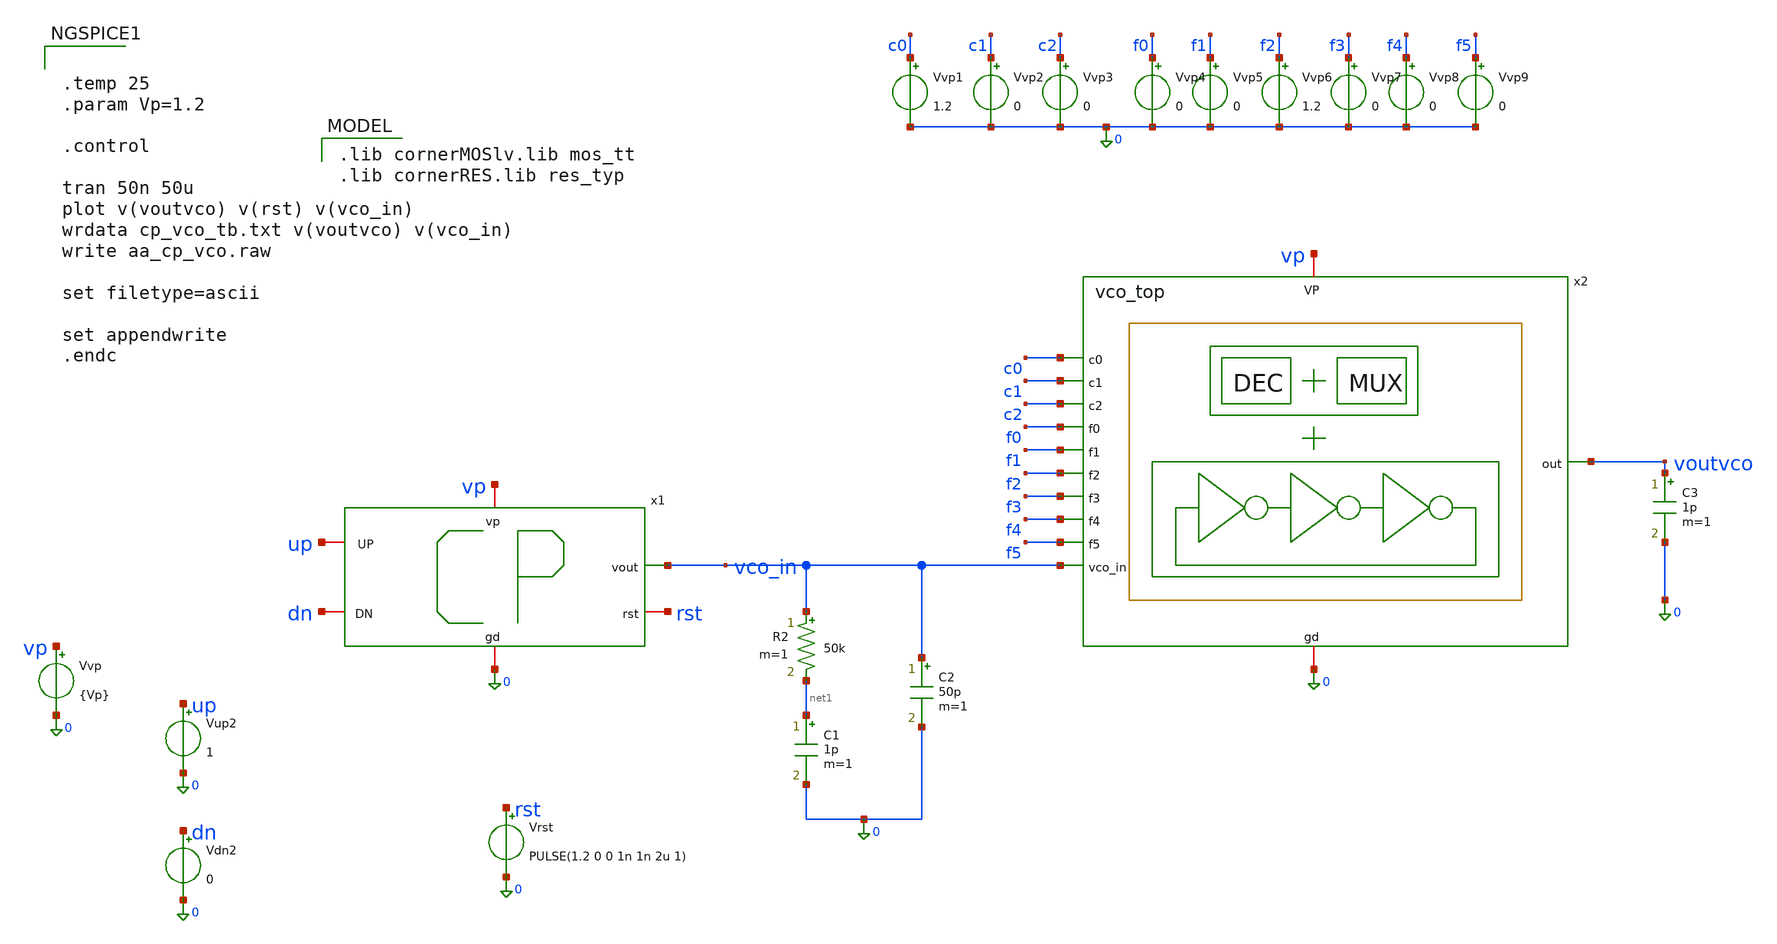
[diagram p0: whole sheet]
** sch_path: schematics/charge_pump/cp10u_fullvco_tb.sch
**.subckt cp10u_fullvco_tb
R2 vco_in net1 50k m=1
C1 net1 0 1p m=1
C2 vco_in 0 50p m=1
Vvp vp 0 {Vp}
Vup2 up 0 1
Vdn2 dn 0 0
Vvp1 c0 0 1.2
Vvp2 c1 0 0
Vvp3 c2 0 0
Vvp4 f0 0 0
Vvp5 f1 0 0
Vvp6 f2 0 1.2
Vvp7 f3 0 0
Vvp8 f4 0 0
Vrst rst 0 PULSE(1.2 0 0 1n 1n 2u 1)
Vvp9 f5 0 0
x2 voutvco 0 vp c0 c1 c2 f0 f1 f2 f3 f4 f5 vco_in vco_top
C3 voutvco 0 1p m=1
x1 vp up vco_in dn rst 0 charge_pump_cell
**** begin user architecture code
 .lib cornerMOSlv.lib mos_tt
.lib cornerRES.lib res_typ






.temp 25
.param Vp=1.2

.control

tran 50n 50u
plot v(voutvco) v(rst) v(vco_in)
wrdata cp_vco_tb.txt v(voutvco) v(vco_in)
write aa_cp_vco.raw

set filetype=ascii

set appendwrite
.endc


**** end user architecture code
**.ends
.end
